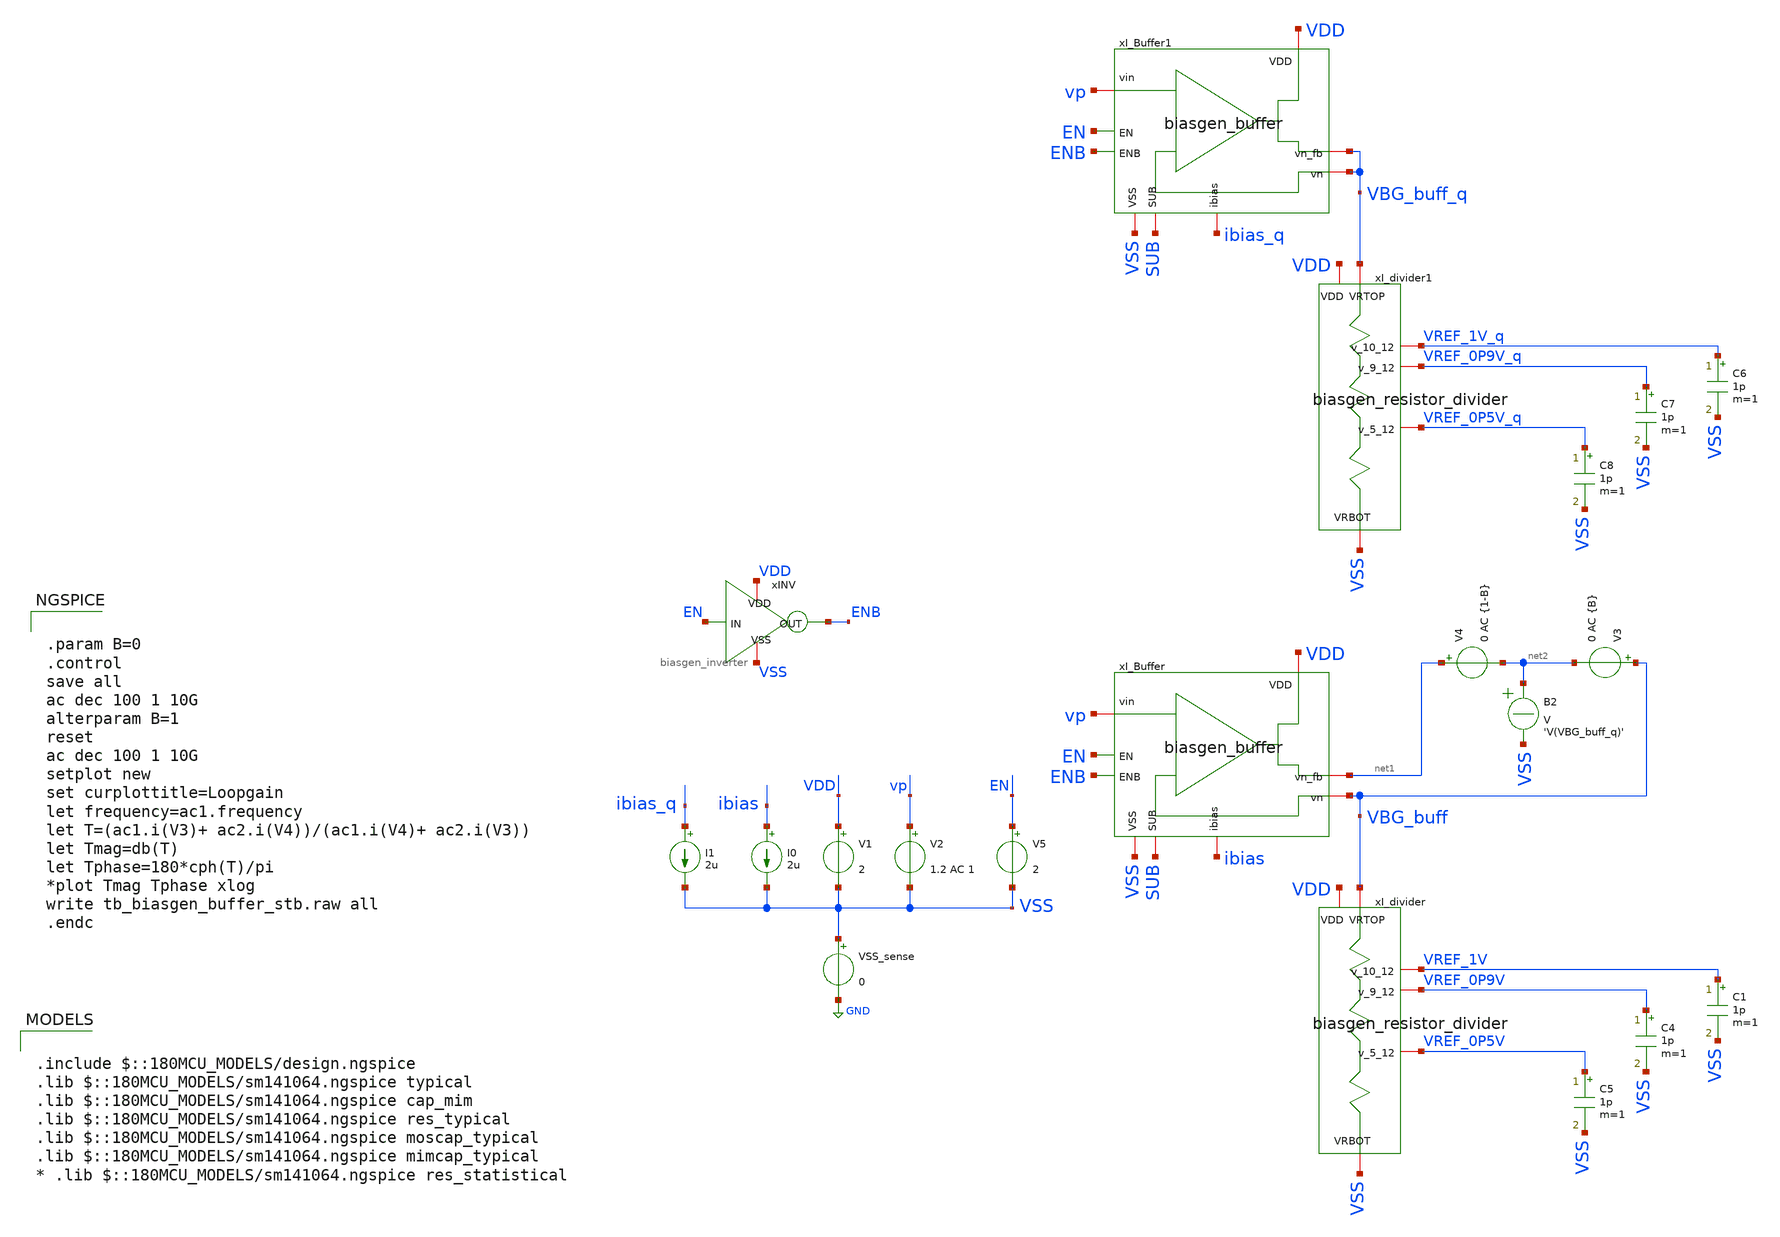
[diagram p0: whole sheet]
** sch_path: designs/libs/tb_biasgen/tb_biasgen_buffer_stb/tb_biasgen_buffer_stb.sch
**.subckt tb_biasgen_buffer_stb
V1 VDD VSS 2
V2 vp VSS 1.2 AC 1
VSS_sense VSS GND 0
I0 ibias VSS 2u
I1 ibias_q VSS 2u
xI_Buffer VDD EN ENB vp SUB ibias net1 VBG_buff VSS biasgen_buffer
xI_divider VBG_buff VDD VREF_1V VREF_0P9V VREF_0P5V VSS biasgen_resistor_divider
xINV VDD EN ENB VSS biasgen_inverter
V4 net1 net2 0 AC {1-B}
B2 net2 VSS V = 'V(VBG_buff_q)'
V3 VBG_buff net2 0 AC {B}
C1 VREF_1V VSS 1p m=1
C4 VREF_0P9V VSS 1p m=1
C5 VREF_0P5V VSS 1p m=1
xI_Buffer1 VDD EN ENB vp SUB ibias_q VBG_buff_q VBG_buff_q VSS biasgen_buffer
xI_divider1 VBG_buff_q VDD VREF_1V_q VREF_0P9V_q VREF_0P5V_q VSS biasgen_resistor_divider
C6 VREF_1V_q VSS 1p m=1
C7 VREF_0P9V_q VSS 1p m=1
C8 VREF_0P5V_q VSS 1p m=1
V5 EN VSS 2
**** begin user architecture code

.include $::180MCU_MODELS/design.ngspice
.lib $::180MCU_MODELS/sm141064.ngspice typical
.lib $::180MCU_MODELS/sm141064.ngspice cap_mim
.lib $::180MCU_MODELS/sm141064.ngspice res_typical
.lib $::180MCU_MODELS/sm141064.ngspice moscap_typical
.lib $::180MCU_MODELS/sm141064.ngspice mimcap_typical
* .lib $::180MCU_MODELS/sm141064.ngspice res_statistical



.param B=0
.control
save all
ac dec 100 1 10G
alterparam B=1
reset
ac dec 100 1 10G
setplot new
set curplottitle=Loopgain
let frequency=ac1.frequency
let T=(ac1.i(V3)+ ac2.i(V4))/(ac1.i(V4)+ ac2.i(V3))
let Tmag=db(T)
let Tphase=180*cph(T)/pi
*plot Tmag Tphase xlog
write tb_biasgen_buffer_stb.raw all
.endc


**** end user architecture code
**.ends
.GLOBAL GND
.end
